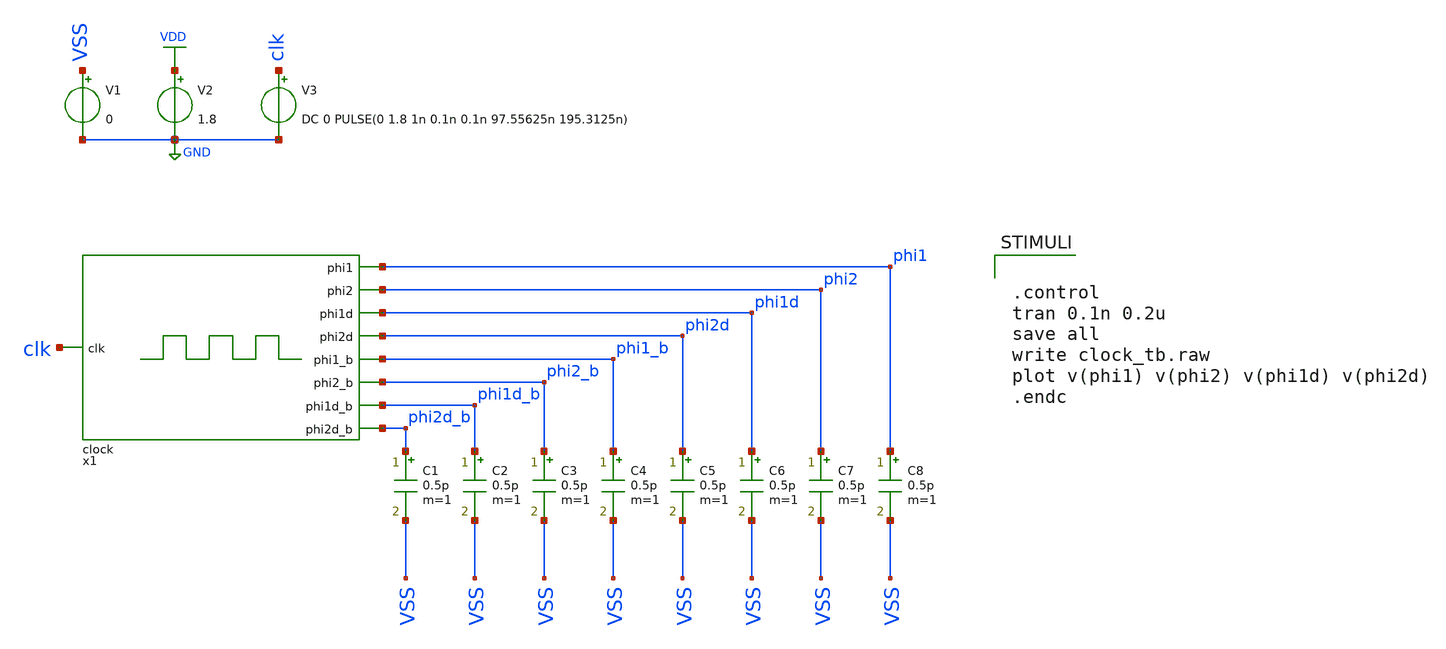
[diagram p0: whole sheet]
** sch_path: verification/schematic/clock_tb.sch
**.subckt clock_tb
x1 phi2 phi2_b phi2d clk phi2d_b phi1d_b phi1d phi1_b phi1 VDD VSS clock
V1 VSS GND 0
V2 VDD GND 1.8
V3 clk GND DC 0 PULSE(0 1.8 1n 0.1n 0.1n 97.55625n 195.3125n)
C1 phi2d_b VSS 0.5p m=1
C2 phi1d_b VSS 0.5p m=1
C3 phi2_b VSS 0.5p m=1
C4 phi1_b VSS 0.5p m=1
C5 phi2d VSS 0.5p m=1
C6 phi1d VSS 0.5p m=1
C7 phi2 VSS 0.5p m=1
C8 phi1 VSS 0.5p m=1
**** begin user architecture code

** opencircuitdesign pdks install
.lib /farmshare/home/classes/ee/372/PDKs/open_pdks_1.0.310/sky130/sky130A/libs.tech/ngspice/sky130.lib.spice tt
.inc /farmshare/home/classes/ee/372/PDKs/open_pdks_1.0.310/sky130/sky130A/libs.ref/sky130_fd_sc_hd/spice/sky130_fd_sc_hd.spice



.control
tran 0.1n 0.2u
save all
write clock_tb.raw
plot v(phi1) v(phi2) v(phi1d) v(phi2d)
.endc


**** end user architecture code
**.ends

* expanding   symbol:  clock.sym # of pins=9
** sym_path: design/schematic/clock.sym
** sch_path: design/schematic/clock.sch
.subckt clock phi2 phi2_b phi2d clk phi2d_b phi1d_b phi1d phi1_b phi1 VDD VSS
*.ipin clk
*.opin phi2d_b
*.opin phi2d
*.opin phi2_b
*.opin phi2
*.opin phi1d_b
*.opin phi1d
*.opin phi1_b
*.opin phi1
x2 clk net5 GND GND VDD VDD net1 sky130_fd_sc_hd__nand2_1
x3 net2 net4 GND GND VDD VDD net3 sky130_fd_sc_hd__nand2_1
x4 net1 GND GND VDD VDD phi2 sky130_fd_sc_hd__clkinv_4
x6 phi2 GND GND VDD VDD net6 sky130_fd_sc_hd__clkinv_1
x9 net3 GND GND VDD VDD phi1 sky130_fd_sc_hd__clkinv_4
x11 phi1 GND GND VDD VDD net7 sky130_fd_sc_hd__clkinv_1
x1 clk GND GND VDD VDD net2 sky130_fd_sc_hd__clkinv_1
x20 net8 GND GND VDD VDD net5 sky130_fd_sc_hd__clkdlybuf4s50_1
x21 net9 GND GND VDD VDD net4 sky130_fd_sc_hd__clkdlybuf4s50_1
x22 net6 GND GND VDD VDD net10 sky130_fd_sc_hd__clkdlybuf4s50_1
x25 net7 GND GND VDD VDD net11 sky130_fd_sc_hd__clkdlybuf4s50_1
x7 net12 GND GND VDD VDD net8 sky130_fd_sc_hd__clkdlybuf4s50_1
x12 net13 GND GND VDD VDD net9 sky130_fd_sc_hd__clkdlybuf4s50_1
x14 net10 GND GND VDD VDD net14 sky130_fd_sc_hd__clkdlybuf4s50_1
x15 net11 GND GND VDD VDD net15 sky130_fd_sc_hd__clkdlybuf4s50_1
x16 net16 GND GND VDD VDD net12 sky130_fd_sc_hd__clkdlybuf4s50_1
x17 net17 GND GND VDD VDD net13 sky130_fd_sc_hd__clkdlybuf4s50_1
x18 net14 GND GND VDD VDD net18 sky130_fd_sc_hd__clkdlybuf4s50_1
x19 net15 GND GND VDD VDD net19 sky130_fd_sc_hd__clkdlybuf4s50_1
x23 net20 GND GND VDD VDD net16 sky130_fd_sc_hd__clkdlybuf4s50_1
x24 net21 GND GND VDD VDD net17 sky130_fd_sc_hd__clkdlybuf4s50_1
x26 net18 GND GND VDD VDD phi2d_b sky130_fd_sc_hd__clkdlybuf4s50_1
x27 net19 GND GND VDD VDD phi1d_b sky130_fd_sc_hd__clkdlybuf4s50_1
x28 net22 GND GND VDD VDD net20 sky130_fd_sc_hd__clkdlybuf4s50_1
x29 net23 GND GND VDD VDD net21 sky130_fd_sc_hd__clkdlybuf4s50_1
x32 net24 GND GND VDD VDD net22 sky130_fd_sc_hd__clkdlybuf4s50_1
x33 net25 GND GND VDD VDD net23 sky130_fd_sc_hd__clkdlybuf4s50_1
x36 net26 GND GND VDD VDD net24 sky130_fd_sc_hd__clkdlybuf4s50_1
x37 net27 GND GND VDD VDD net25 sky130_fd_sc_hd__clkdlybuf4s50_1
x40 net28 GND GND VDD VDD net26 sky130_fd_sc_hd__clkdlybuf4s50_1
x41 net29 GND GND VDD VDD net27 sky130_fd_sc_hd__clkdlybuf4s50_1
x44 net30 GND GND VDD VDD net28 sky130_fd_sc_hd__clkdlybuf4s50_1
x45 net31 GND GND VDD VDD net29 sky130_fd_sc_hd__clkdlybuf4s50_1
x48 net32 GND GND VDD VDD net30 sky130_fd_sc_hd__clkdlybuf4s50_1
x49 net33 GND GND VDD VDD net31 sky130_fd_sc_hd__clkdlybuf4s50_1
x52 net34 GND GND VDD VDD net32 sky130_fd_sc_hd__clkdlybuf4s50_1
x53 net35 GND GND VDD VDD net33 sky130_fd_sc_hd__clkdlybuf4s50_1
x56 net36 GND GND VDD VDD net34 sky130_fd_sc_hd__clkdlybuf4s50_1
x57 net37 GND GND VDD VDD net35 sky130_fd_sc_hd__clkdlybuf4s50_1
x60 net38 GND GND VDD VDD net36 sky130_fd_sc_hd__clkdlybuf4s50_1
x61 net39 GND GND VDD VDD net37 sky130_fd_sc_hd__clkdlybuf4s50_1
x64 net40 GND GND VDD VDD net38 sky130_fd_sc_hd__clkdlybuf4s50_1
x65 net41 GND GND VDD VDD net39 sky130_fd_sc_hd__clkdlybuf4s50_1
x68 net42 GND GND VDD VDD net40 sky130_fd_sc_hd__clkdlybuf4s50_1
x69 net43 GND GND VDD VDD net41 sky130_fd_sc_hd__clkdlybuf4s50_1
x72 net44 GND GND VDD VDD net42 sky130_fd_sc_hd__clkdlybuf4s50_1
x73 net45 GND GND VDD VDD net43 sky130_fd_sc_hd__clkdlybuf4s50_1
x76 net46 GND GND VDD VDD net44 sky130_fd_sc_hd__clkdlybuf4s50_1
x77 net47 GND GND VDD VDD net45 sky130_fd_sc_hd__clkdlybuf4s50_1
x80 net48 GND GND VDD VDD net46 sky130_fd_sc_hd__clkdlybuf4s50_1
x81 net49 GND GND VDD VDD net47 sky130_fd_sc_hd__clkdlybuf4s50_1
x84 net50 GND GND VDD VDD net48 sky130_fd_sc_hd__clkdlybuf4s50_1
x85 net51 GND GND VDD VDD net49 sky130_fd_sc_hd__clkdlybuf4s50_1
x86 net52 GND GND VDD VDD net50 sky130_fd_sc_hd__clkdlybuf4s50_1
x87 net53 GND GND VDD VDD net51 sky130_fd_sc_hd__clkdlybuf4s50_1
x88 net54 GND GND VDD VDD net52 sky130_fd_sc_hd__clkdlybuf4s50_1
x89 net55 GND GND VDD VDD net53 sky130_fd_sc_hd__clkdlybuf4s50_1
x90 net56 GND GND VDD VDD net54 sky130_fd_sc_hd__clkdlybuf4s50_1
x91 net57 GND GND VDD VDD net55 sky130_fd_sc_hd__clkdlybuf4s50_1
x92 net58 GND GND VDD VDD net56 sky130_fd_sc_hd__clkdlybuf4s50_1
x93 net59 GND GND VDD VDD net57 sky130_fd_sc_hd__clkdlybuf4s50_1
x94 net60 GND GND VDD VDD net58 sky130_fd_sc_hd__clkdlybuf4s50_1
x95 net61 GND GND VDD VDD net59 sky130_fd_sc_hd__clkdlybuf4s50_1
x96 net62 GND GND VDD VDD net60 sky130_fd_sc_hd__clkdlybuf4s50_1
x97 net63 GND GND VDD VDD net61 sky130_fd_sc_hd__clkdlybuf4s50_1
x98 net64 GND GND VDD VDD net62 sky130_fd_sc_hd__clkdlybuf4s50_1
x99 net65 GND GND VDD VDD net63 sky130_fd_sc_hd__clkdlybuf4s50_1
x100 net66 GND GND VDD VDD net64 sky130_fd_sc_hd__clkdlybuf4s50_1
x101 net67 GND GND VDD VDD net65 sky130_fd_sc_hd__clkdlybuf4s50_1
x102 net68 GND GND VDD VDD net66 sky130_fd_sc_hd__clkdlybuf4s50_1
x103 net69 GND GND VDD VDD net67 sky130_fd_sc_hd__clkdlybuf4s50_1
x104 net70 GND GND VDD VDD net68 sky130_fd_sc_hd__clkdlybuf4s50_1
x105 net71 GND GND VDD VDD net69 sky130_fd_sc_hd__clkdlybuf4s50_1
x106 net72 GND GND VDD VDD net70 sky130_fd_sc_hd__clkdlybuf4s50_1
x107 net73 GND GND VDD VDD net71 sky130_fd_sc_hd__clkdlybuf4s50_1
x108 net74 GND GND VDD VDD net72 sky130_fd_sc_hd__clkdlybuf4s50_1
x109 net75 GND GND VDD VDD net73 sky130_fd_sc_hd__clkdlybuf4s50_1
x110 net76 GND GND VDD VDD net74 sky130_fd_sc_hd__clkdlybuf4s50_1
x111 net77 GND GND VDD VDD net75 sky130_fd_sc_hd__clkdlybuf4s50_1
x112 net78 GND GND VDD VDD net76 sky130_fd_sc_hd__clkdlybuf4s50_1
x113 net79 GND GND VDD VDD net77 sky130_fd_sc_hd__clkdlybuf4s50_1
x114 net80 GND GND VDD VDD net78 sky130_fd_sc_hd__clkdlybuf4s50_1
x115 net81 GND GND VDD VDD net79 sky130_fd_sc_hd__clkdlybuf4s50_1
x116 net1 phi2d_b GND GND VDD VDD phi2d sky130_fd_sc_hd__nand2_4
x5 phi2 GND GND VDD VDD phi2_b sky130_fd_sc_hd__clkinv_1
x10 phi1 GND GND VDD VDD phi1_b sky130_fd_sc_hd__clkinv_1
x117 net3 phi1d_b GND GND VDD VDD phi1d sky130_fd_sc_hd__nand2_4
x8 net82 GND GND VDD VDD net80 sky130_fd_sc_hd__clkdlybuf4s50_1
x13 net83 GND GND VDD VDD net81 sky130_fd_sc_hd__clkdlybuf4s50_1
x118 net84 GND GND VDD VDD net82 sky130_fd_sc_hd__clkdlybuf4s50_1
x119 net85 GND GND VDD VDD net83 sky130_fd_sc_hd__clkdlybuf4s50_1
x120 net86 GND GND VDD VDD net84 sky130_fd_sc_hd__clkdlybuf4s50_1
x121 net87 GND GND VDD VDD net85 sky130_fd_sc_hd__clkdlybuf4s50_1
x122 net88 GND GND VDD VDD net86 sky130_fd_sc_hd__clkdlybuf4s50_1
x123 net89 GND GND VDD VDD net87 sky130_fd_sc_hd__clkdlybuf4s50_1
x124 net90 GND GND VDD VDD net88 sky130_fd_sc_hd__clkdlybuf4s50_1
x125 net91 GND GND VDD VDD net89 sky130_fd_sc_hd__clkdlybuf4s50_1
x126 net92 GND GND VDD VDD net90 sky130_fd_sc_hd__clkdlybuf4s50_1
x127 net93 GND GND VDD VDD net91 sky130_fd_sc_hd__clkdlybuf4s50_1
x128 net94 GND GND VDD VDD net92 sky130_fd_sc_hd__clkdlybuf4s50_1
x129 net95 GND GND VDD VDD net93 sky130_fd_sc_hd__clkdlybuf4s50_1
x130 phi1d_b GND GND VDD VDD net96 sky130_fd_sc_hd__clkdlybuf4s50_1
x131 phi2d_b GND GND VDD VDD net97 sky130_fd_sc_hd__clkdlybuf4s50_1
x78 net98 GND GND VDD VDD net94 sky130_fd_sc_hd__clkdlybuf4s50_1
x79 net99 GND GND VDD VDD net95 sky130_fd_sc_hd__clkdlybuf4s50_1
x82 net100 GND GND VDD VDD net98 sky130_fd_sc_hd__clkdlybuf4s50_1
x83 net101 GND GND VDD VDD net99 sky130_fd_sc_hd__clkdlybuf4s50_1
x132 net102 GND GND VDD VDD net100 sky130_fd_sc_hd__clkdlybuf4s50_1
x133 net103 GND GND VDD VDD net101 sky130_fd_sc_hd__clkdlybuf4s50_1
x134 net96 GND GND VDD VDD net102 sky130_fd_sc_hd__clkdlybuf4s50_1
x135 net97 GND GND VDD VDD net103 sky130_fd_sc_hd__clkdlybuf4s50_1
.ends

.GLOBAL GND
.GLOBAL VDD
.end
